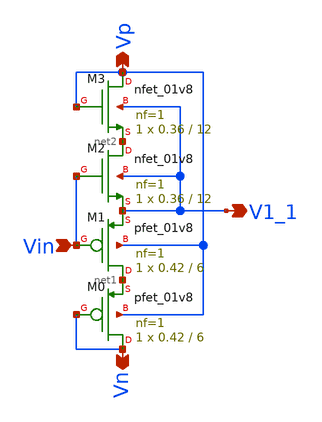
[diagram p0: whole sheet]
** sch_path: xschem/Vth_sch/Symbol/th01_test.sch
**.subckt th01_test Vn Vp Vin V1_1
*.opin Vn
*.opin Vp
*.ipin Vin
*.opin V1_1
XM0 Vn Vn net1 Vp sky130_fd_pr__pfet_01v8 L=6 W=0.42 nf=1 ad='int((nf+1)/2) * W/nf * 0.29' as='int((nf+2)/2) * W/nf * 0.29'
+ pd='2*int((nf+1)/2) * (W/nf + 0.29)' ps='2*int((nf+2)/2) * (W/nf + 0.29)' nrd='0.29 / W' nrs='0.29 / W'
+ sa=0 sb=0 sd=0 mult=1 m=1
XM3 Vp Vp net2 V1_1 sky130_fd_pr__nfet_01v8 L=12 W=0.36 nf=1 ad='int((nf+1)/2) * W/nf * 0.29' as='int((nf+2)/2) * W/nf * 0.29'
+ pd='2*int((nf+1)/2) * (W/nf + 0.29)' ps='2*int((nf+2)/2) * (W/nf + 0.29)' nrd='0.29 / W' nrs='0.29 / W'
+ sa=0 sb=0 sd=0 mult=1 m=1
XM1 net1 Vin V1_1 Vp sky130_fd_pr__pfet_01v8 L=6 W=0.42 nf=1 ad='int((nf+1)/2) * W/nf * 0.29' as='int((nf+2)/2) * W/nf * 0.29'
+ pd='2*int((nf+1)/2) * (W/nf + 0.29)' ps='2*int((nf+2)/2) * (W/nf + 0.29)' nrd='0.29 / W' nrs='0.29 / W'
+ sa=0 sb=0 sd=0 mult=1 m=1
XM2 net2 Vin V1_1 V1_1 sky130_fd_pr__nfet_01v8 L=12 W=0.36 nf=1 ad='int((nf+1)/2) * W/nf * 0.29' as='int((nf+2)/2) * W/nf * 0.29'
+ pd='2*int((nf+1)/2) * (W/nf + 0.29)' ps='2*int((nf+2)/2) * (W/nf + 0.29)' nrd='0.29 / W' nrs='0.29 / W'
+ sa=0 sb=0 sd=0 mult=1 m=1
**.ends
.end
